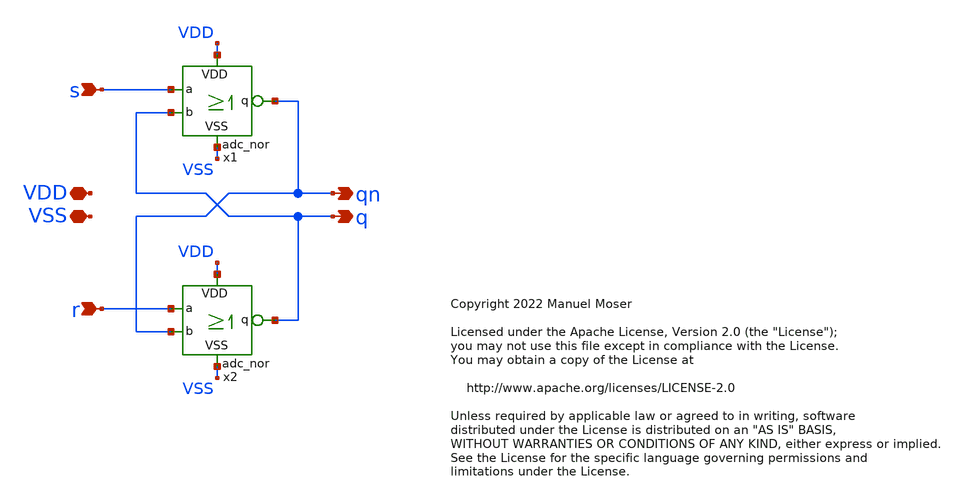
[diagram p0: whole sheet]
** sch_path: xschem/adc_nor_latch.sch
* Copyright 2022 Manuel Moser
* Licensed under the Apache License, Version 2.0 (the "License");
**.subckt adc_nor_latch VDD VSS s r q qn
*.iopin VDD
*.iopin VSS
*.ipin s
*.ipin r
*.opin q
*.opin qn
x1 q s VDD qn VSS adc_nor
x2 qn r VDD q VSS adc_nor
**.ends

* expanding   symbol:  adc_nor.sym # of pins=5
** sym_path: xschem/adc_nor.sym
** sch_path: xschem/adc_nor.sch
.subckt adc_nor b a VDD q VSS
*.iopin VDD
*.iopin VSS
*.ipin b
*.ipin a
*.opin q
XM5 q b VSS VSS sky130_fd_pr__nfet_01v8 L=0.15 W=0.42 nf=1 ad='int((nf+1)/2) * W/nf * 0.29' as='int((nf+2)/2) * W/nf * 0.29'
+ pd='2*int((nf+1)/2) * (W/nf + 0.29)' ps='2*int((nf+2)/2) * (W/nf + 0.29)' nrd='0.29 / W' nrs='0.29 / W'
+ sa=0 sb=0 sd=0 mult=1 m=1
XM6 q a VSS VSS sky130_fd_pr__nfet_01v8 L=0.15 W=0.42 nf=1 ad='int((nf+1)/2) * W/nf * 0.29' as='int((nf+2)/2) * W/nf * 0.29'
+ pd='2*int((nf+1)/2) * (W/nf + 0.29)' ps='2*int((nf+2)/2) * (W/nf + 0.29)' nrd='0.29 / W' nrs='0.29 / W'
+ sa=0 sb=0 sd=0 mult=1 m=1
XM1 q b net1 VDD sky130_fd_pr__pfet_01v8 L=0.15 W=0.8 nf=1 ad='int((nf+1)/2) * W/nf * 0.29' as='int((nf+2)/2) * W/nf * 0.29'
+ pd='2*int((nf+1)/2) * (W/nf + 0.29)' ps='2*int((nf+2)/2) * (W/nf + 0.29)' nrd='0.29 / W' nrs='0.29 / W'
+ sa=0 sb=0 sd=0 mult=1 m=1
XM2 q a net2 VDD sky130_fd_pr__pfet_01v8 L=0.15 W=0.8 nf=1 ad='int((nf+1)/2) * W/nf * 0.29' as='int((nf+2)/2) * W/nf * 0.29'
+ pd='2*int((nf+1)/2) * (W/nf + 0.29)' ps='2*int((nf+2)/2) * (W/nf + 0.29)' nrd='0.29 / W' nrs='0.29 / W'
+ sa=0 sb=0 sd=0 mult=1 m=1
XM3 net2 b VDD VDD sky130_fd_pr__pfet_01v8 L=0.15 W=0.8 nf=1 ad='int((nf+1)/2) * W/nf * 0.29' as='int((nf+2)/2) * W/nf * 0.29'
+ pd='2*int((nf+1)/2) * (W/nf + 0.29)' ps='2*int((nf+2)/2) * (W/nf + 0.29)' nrd='0.29 / W' nrs='0.29 / W'
+ sa=0 sb=0 sd=0 mult=1 m=1
XM4 net1 a VDD VDD sky130_fd_pr__pfet_01v8 L=0.15 W=0.8 nf=1 ad='int((nf+1)/2) * W/nf * 0.29' as='int((nf+2)/2) * W/nf * 0.29'
+ pd='2*int((nf+1)/2) * (W/nf + 0.29)' ps='2*int((nf+2)/2) * (W/nf + 0.29)' nrd='0.29 / W' nrs='0.29 / W'
+ sa=0 sb=0 sd=0 mult=1 m=1
.ends

.end
